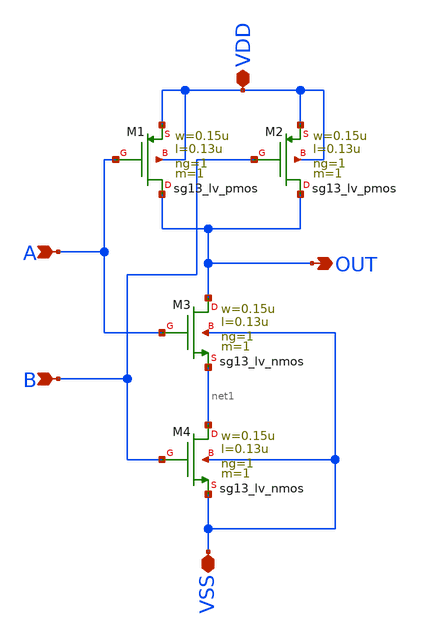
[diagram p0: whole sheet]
** sch_path: nand2l.sch
**.subckt nand2l A B OUT VSS VDD
*.ipin A
*.ipin B
*.opin OUT
*.iopin VSS
*.iopin VDD
XM1 OUT A VDD VDD sg13_lv_pmos w=0.15u l=0.13u ng=1 m=1 mm_ok=1
XM2 OUT B VDD VDD sg13_lv_pmos w=0.15u l=0.13u ng=1 m=1 mm_ok=1
XM3 OUT A net1 VSS sg13_lv_nmos w=0.15u l=0.13u ng=1 m=1 mm_ok=1
XM4 net1 B VSS VSS sg13_lv_nmos w=0.15u l=0.13u ng=1 m=1 mm_ok=1
**.ends
.end
